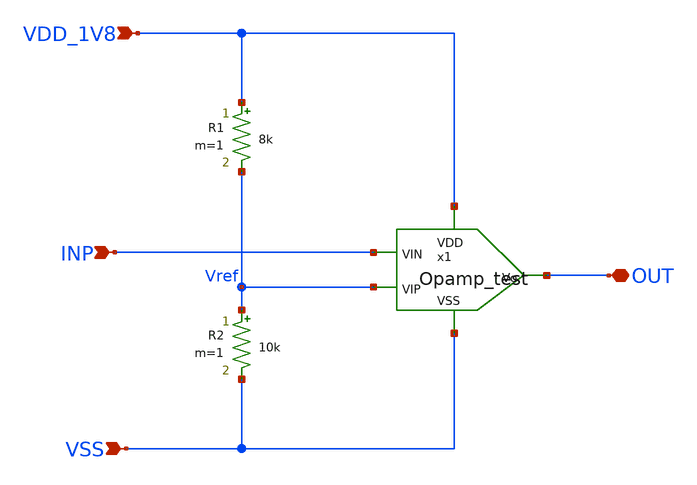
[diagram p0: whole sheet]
** sch_path: design/JNW_GR04_SKY130A/Comparator.sch
**.subckt Comparator VDD_1V8 INP VSS OUT
*.ipin VDD_1V8
*.ipin INP
*.ipin VSS
*.iopin OUT
x1 VDD_1V8 INP Vref OUT VSS Opamp_test
R1 VDD_1V8 Vref 8k m=1
R2 Vref VSS 10k m=1
**.ends
.end
